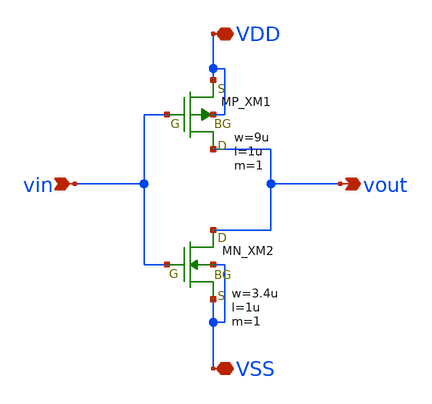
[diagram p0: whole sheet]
** sch_path: member_project/inverter/sanken/july_fifth/inverter_july_fifth.sch
**.subckt inverter_july_fifth vout vin VSS VDD
*.opin vout
*.ipin vin
*.iopin VSS
*.iopin VDD
XXM1 vout vin VDD VDD PMOS w=9u l=1u nrd=0 nrs=0 m=1
XXM2 vout vin VSS VSS NMOS w=3.4u l=1u nrd=0 nrs=0 m=1
**.ends
.end
